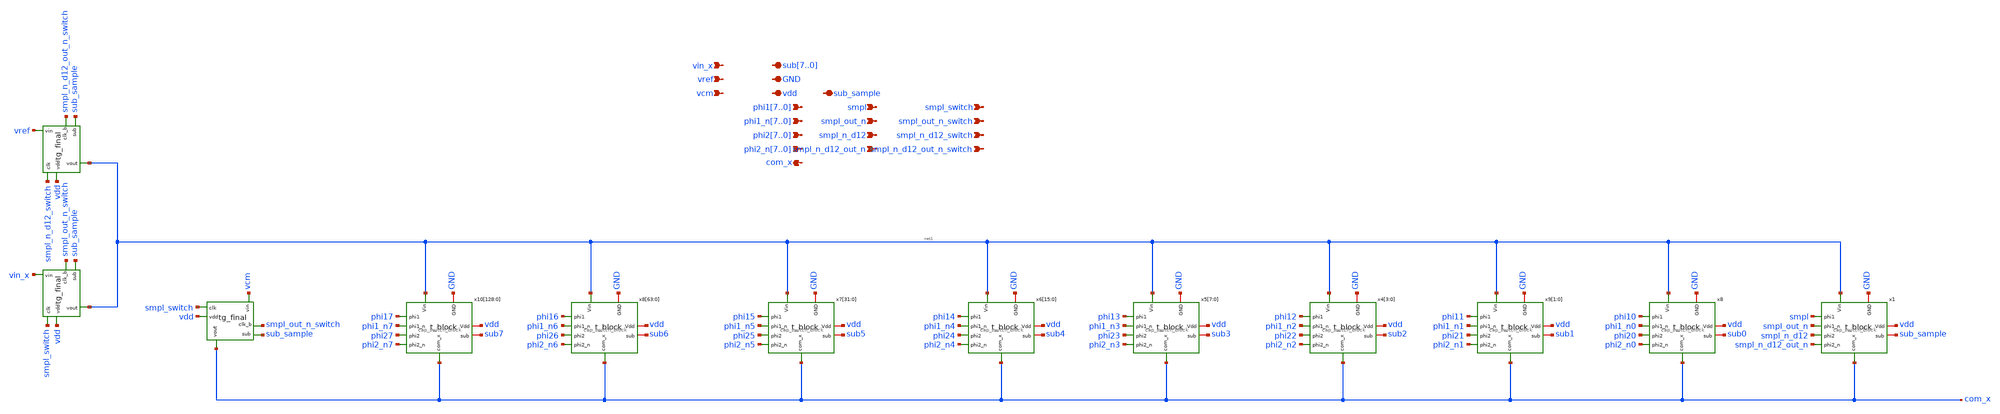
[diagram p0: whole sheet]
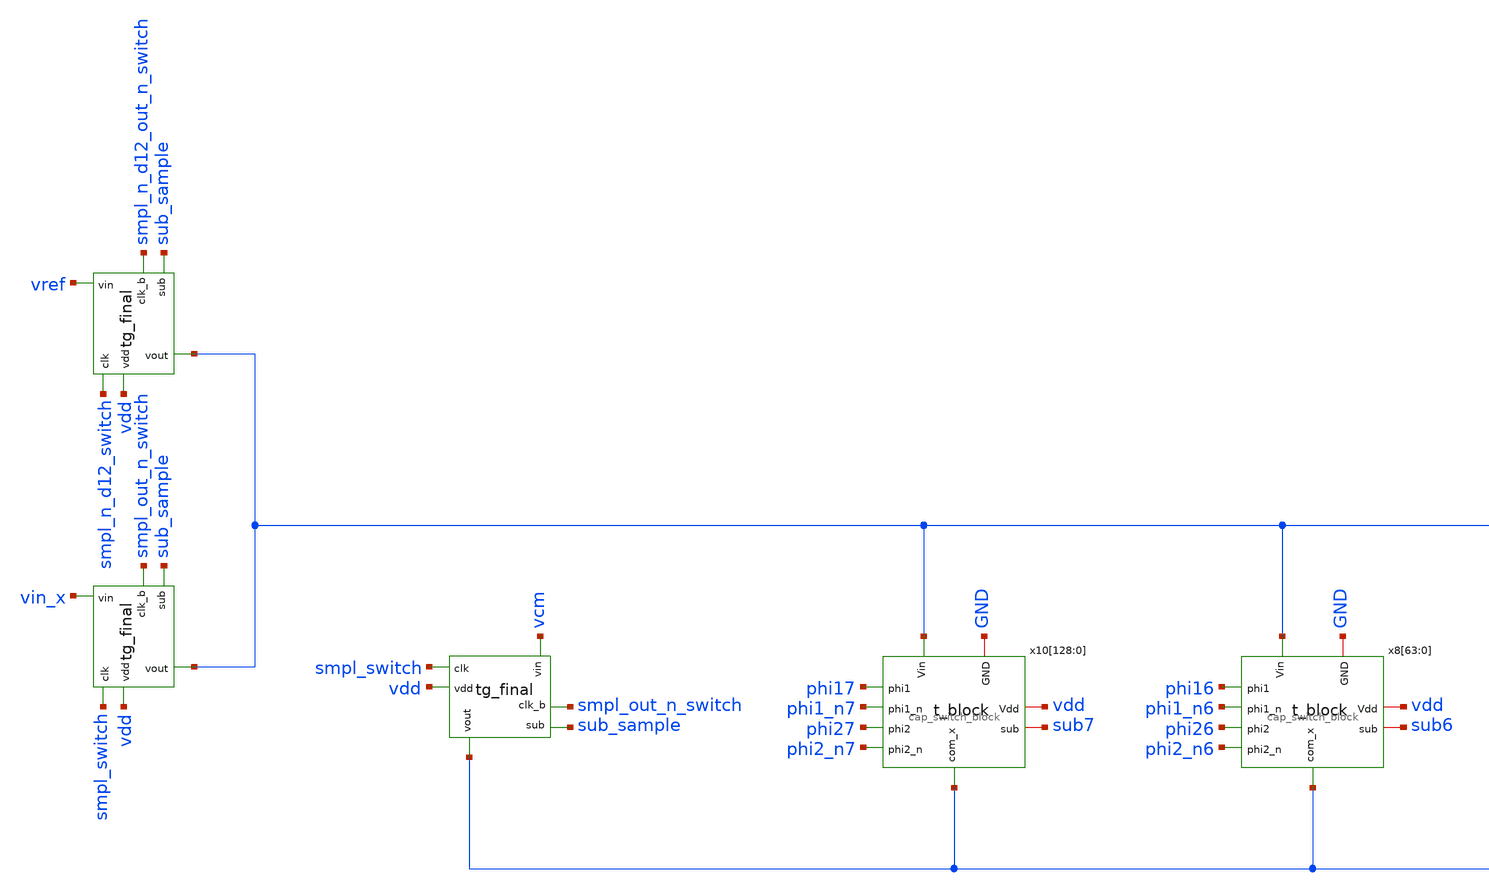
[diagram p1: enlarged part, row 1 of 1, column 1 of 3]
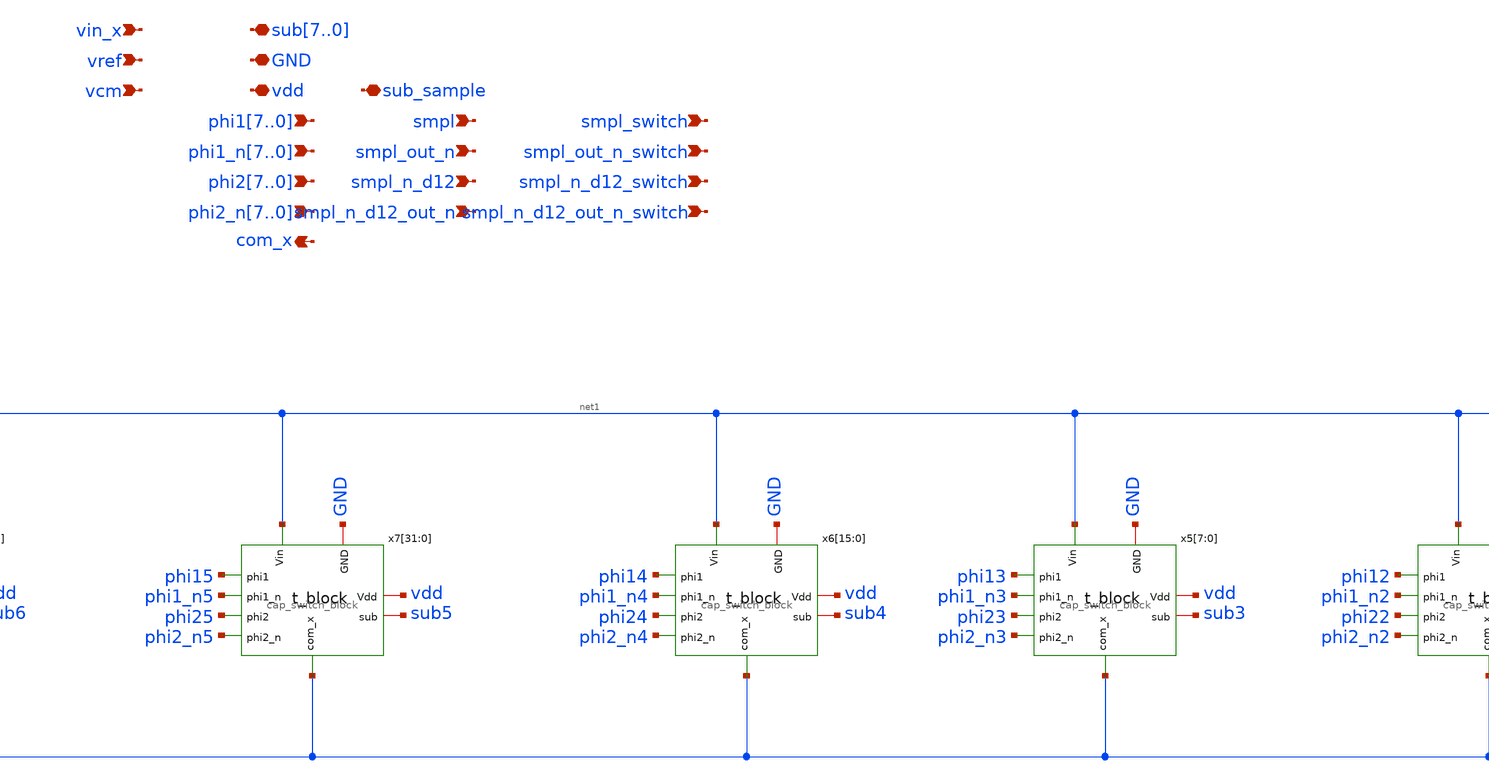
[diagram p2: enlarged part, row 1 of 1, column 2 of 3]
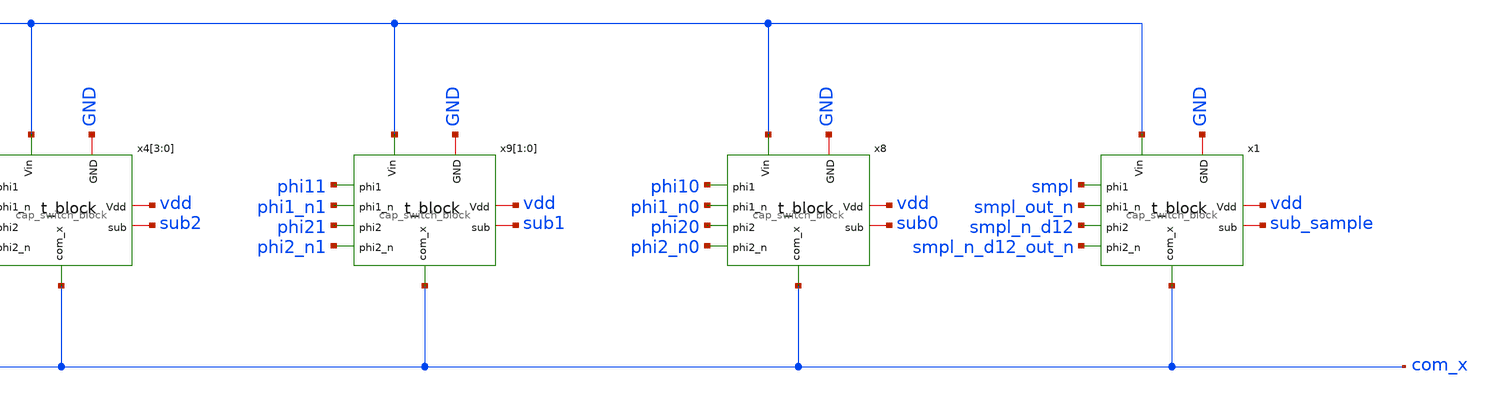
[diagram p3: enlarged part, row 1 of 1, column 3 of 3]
** sch_path: test/design/capdac_switches.sch
**.subckt capdac_switches phi17,phi16,phi15,phi14,phi13,phi12,phi11,phi10
*+ phi1_n7,phi1_n6,phi1_n5,phi1_n4,phi1_n3,phi1_n2,phi1_n1,phi1_n0 vdd GND sub7,sub6,sub5,sub4,sub3,sub2,sub1,sub0 phi27,phi26,phi25,phi24,phi23,phi22,phi21,phi20
*+ phi2_n7,phi2_n6,phi2_n5,phi2_n4,phi2_n3,phi2_n2,phi2_n1,phi2_n0 com_x smpl smpl_out_n smpl_n_d12 smpl_n_d12_out_n sub_sample vcm vref vin_x smpl_switch
*+ smpl_out_n_switch smpl_n_d12_switch smpl_n_d12_out_n_switch
*.ipin phi17,phi16,phi15,phi14,phi13,phi12,phi11,phi10
*.ipin phi1_n7,phi1_n6,phi1_n5,phi1_n4,phi1_n3,phi1_n2,phi1_n1,phi1_n0
*.iopin vdd
*.iopin GND
*.iopin sub7,sub6,sub5,sub4,sub3,sub2,sub1,sub0
*.ipin phi27,phi26,phi25,phi24,phi23,phi22,phi21,phi20
*.ipin phi2_n7,phi2_n6,phi2_n5,phi2_n4,phi2_n3,phi2_n2,phi2_n1,phi2_n0
*.opin com_x
*.ipin smpl
*.ipin smpl_out_n
*.ipin smpl_n_d12
*.ipin smpl_n_d12_out_n
*.iopin sub_sample
*.ipin vcm
*.ipin vref
*.ipin vin_x
*.ipin smpl_switch
*.ipin smpl_out_n_switch
*.ipin smpl_n_d12_switch
*.ipin smpl_n_d12_out_n_switch
x8 net1 sub0 GND vdd phi10 phi20 phi2_n0 phi1_n0 com_x cap_switch_block
x9[1] net1 sub1 GND vdd phi11 phi21 phi2_n1 phi1_n1 com_x cap_switch_block
x9[0] net1 sub1 GND vdd phi11 phi21 phi2_n1 phi1_n1 com_x cap_switch_block
x4[3] net1 sub2 GND vdd phi12 phi22 phi2_n2 phi1_n2 com_x cap_switch_block
x4[2] net1 sub2 GND vdd phi12 phi22 phi2_n2 phi1_n2 com_x cap_switch_block
x4[1] net1 sub2 GND vdd phi12 phi22 phi2_n2 phi1_n2 com_x cap_switch_block
x4[0] net1 sub2 GND vdd phi12 phi22 phi2_n2 phi1_n2 com_x cap_switch_block
x5[7] net1 sub3 GND vdd phi13 phi23 phi2_n3 phi1_n3 com_x cap_switch_block
x5[6] net1 sub3 GND vdd phi13 phi23 phi2_n3 phi1_n3 com_x cap_switch_block
x5[5] net1 sub3 GND vdd phi13 phi23 phi2_n3 phi1_n3 com_x cap_switch_block
x5[4] net1 sub3 GND vdd phi13 phi23 phi2_n3 phi1_n3 com_x cap_switch_block
x5[3] net1 sub3 GND vdd phi13 phi23 phi2_n3 phi1_n3 com_x cap_switch_block
x5[2] net1 sub3 GND vdd phi13 phi23 phi2_n3 phi1_n3 com_x cap_switch_block
x5[1] net1 sub3 GND vdd phi13 phi23 phi2_n3 phi1_n3 com_x cap_switch_block
x5[0] net1 sub3 GND vdd phi13 phi23 phi2_n3 phi1_n3 com_x cap_switch_block
x6[15] net1 sub4 GND vdd phi14 phi24 phi2_n4 phi1_n4 com_x cap_switch_block
x6[14] net1 sub4 GND vdd phi14 phi24 phi2_n4 phi1_n4 com_x cap_switch_block
x6[13] net1 sub4 GND vdd phi14 phi24 phi2_n4 phi1_n4 com_x cap_switch_block
x6[12] net1 sub4 GND vdd phi14 phi24 phi2_n4 phi1_n4 com_x cap_switch_block
x6[11] net1 sub4 GND vdd phi14 phi24 phi2_n4 phi1_n4 com_x cap_switch_block
x6[10] net1 sub4 GND vdd phi14 phi24 phi2_n4 phi1_n4 com_x cap_switch_block
x6[9] net1 sub4 GND vdd phi14 phi24 phi2_n4 phi1_n4 com_x cap_switch_block
x6[8] net1 sub4 GND vdd phi14 phi24 phi2_n4 phi1_n4 com_x cap_switch_block
x6[7] net1 sub4 GND vdd phi14 phi24 phi2_n4 phi1_n4 com_x cap_switch_block
x6[6] net1 sub4 GND vdd phi14 phi24 phi2_n4 phi1_n4 com_x cap_switch_block
x6[5] net1 sub4 GND vdd phi14 phi24 phi2_n4 phi1_n4 com_x cap_switch_block
x6[4] net1 sub4 GND vdd phi14 phi24 phi2_n4 phi1_n4 com_x cap_switch_block
x6[3] net1 sub4 GND vdd phi14 phi24 phi2_n4 phi1_n4 com_x cap_switch_block
x6[2] net1 sub4 GND vdd phi14 phi24 phi2_n4 phi1_n4 com_x cap_switch_block
x6[1] net1 sub4 GND vdd phi14 phi24 phi2_n4 phi1_n4 com_x cap_switch_block
x6[0] net1 sub4 GND vdd phi14 phi24 phi2_n4 phi1_n4 com_x cap_switch_block
x7[31] net1 sub5 GND vdd phi15 phi25 phi2_n5 phi1_n5 com_x cap_switch_block
x7[30] net1 sub5 GND vdd phi15 phi25 phi2_n5 phi1_n5 com_x cap_switch_block
x7[29] net1 sub5 GND vdd phi15 phi25 phi2_n5 phi1_n5 com_x cap_switch_block
x7[28] net1 sub5 GND vdd phi15 phi25 phi2_n5 phi1_n5 com_x cap_switch_block
x7[27] net1 sub5 GND vdd phi15 phi25 phi2_n5 phi1_n5 com_x cap_switch_block
x7[26] net1 sub5 GND vdd phi15 phi25 phi2_n5 phi1_n5 com_x cap_switch_block
x7[25] net1 sub5 GND vdd phi15 phi25 phi2_n5 phi1_n5 com_x cap_switch_block
x7[24] net1 sub5 GND vdd phi15 phi25 phi2_n5 phi1_n5 com_x cap_switch_block
x7[23] net1 sub5 GND vdd phi15 phi25 phi2_n5 phi1_n5 com_x cap_switch_block
x7[22] net1 sub5 GND vdd phi15 phi25 phi2_n5 phi1_n5 com_x cap_switch_block
x7[21] net1 sub5 GND vdd phi15 phi25 phi2_n5 phi1_n5 com_x cap_switch_block
x7[20] net1 sub5 GND vdd phi15 phi25 phi2_n5 phi1_n5 com_x cap_switch_block
x7[19] net1 sub5 GND vdd phi15 phi25 phi2_n5 phi1_n5 com_x cap_switch_block
x7[18] net1 sub5 GND vdd phi15 phi25 phi2_n5 phi1_n5 com_x cap_switch_block
x7[17] net1 sub5 GND vdd phi15 phi25 phi2_n5 phi1_n5 com_x cap_switch_block
x7[16] net1 sub5 GND vdd phi15 phi25 phi2_n5 phi1_n5 com_x cap_switch_block
x7[15] net1 sub5 GND vdd phi15 phi25 phi2_n5 phi1_n5 com_x cap_switch_block
x7[14] net1 sub5 GND vdd phi15 phi25 phi2_n5 phi1_n5 com_x cap_switch_block
x7[13] net1 sub5 GND vdd phi15 phi25 phi2_n5 phi1_n5 com_x cap_switch_block
x7[12] net1 sub5 GND vdd phi15 phi25 phi2_n5 phi1_n5 com_x cap_switch_block
x7[11] net1 sub5 GND vdd phi15 phi25 phi2_n5 phi1_n5 com_x cap_switch_block
x7[10] net1 sub5 GND vdd phi15 phi25 phi2_n5 phi1_n5 com_x cap_switch_block
x7[9] net1 sub5 GND vdd phi15 phi25 phi2_n5 phi1_n5 com_x cap_switch_block
x7[8] net1 sub5 GND vdd phi15 phi25 phi2_n5 phi1_n5 com_x cap_switch_block
x7[7] net1 sub5 GND vdd phi15 phi25 phi2_n5 phi1_n5 com_x cap_switch_block
x7[6] net1 sub5 GND vdd phi15 phi25 phi2_n5 phi1_n5 com_x cap_switch_block
x7[5] net1 sub5 GND vdd phi15 phi25 phi2_n5 phi1_n5 com_x cap_switch_block
x7[4] net1 sub5 GND vdd phi15 phi25 phi2_n5 phi1_n5 com_x cap_switch_block
x7[3] net1 sub5 GND vdd phi15 phi25 phi2_n5 phi1_n5 com_x cap_switch_block
x7[2] net1 sub5 GND vdd phi15 phi25 phi2_n5 phi1_n5 com_x cap_switch_block
x7[1] net1 sub5 GND vdd phi15 phi25 phi2_n5 phi1_n5 com_x cap_switch_block
x7[0] net1 sub5 GND vdd phi15 phi25 phi2_n5 phi1_n5 com_x cap_switch_block
x8[63] net1 sub6 GND vdd phi16 phi26 phi2_n6 phi1_n6 com_x cap_switch_block
x8[62] net1 sub6 GND vdd phi16 phi26 phi2_n6 phi1_n6 com_x cap_switch_block
x8[61] net1 sub6 GND vdd phi16 phi26 phi2_n6 phi1_n6 com_x cap_switch_block
x8[60] net1 sub6 GND vdd phi16 phi26 phi2_n6 phi1_n6 com_x cap_switch_block
x8[59] net1 sub6 GND vdd phi16 phi26 phi2_n6 phi1_n6 com_x cap_switch_block
x8[58] net1 sub6 GND vdd phi16 phi26 phi2_n6 phi1_n6 com_x cap_switch_block
x8[57] net1 sub6 GND vdd phi16 phi26 phi2_n6 phi1_n6 com_x cap_switch_block
x8[56] net1 sub6 GND vdd phi16 phi26 phi2_n6 phi1_n6 com_x cap_switch_block
x8[55] net1 sub6 GND vdd phi16 phi26 phi2_n6 phi1_n6 com_x cap_switch_block
x8[54] net1 sub6 GND vdd phi16 phi26 phi2_n6 phi1_n6 com_x cap_switch_block
x8[53] net1 sub6 GND vdd phi16 phi26 phi2_n6 phi1_n6 com_x cap_switch_block
x8[52] net1 sub6 GND vdd phi16 phi26 phi2_n6 phi1_n6 com_x cap_switch_block
x8[51] net1 sub6 GND vdd phi16 phi26 phi2_n6 phi1_n6 com_x cap_switch_block
x8[50] net1 sub6 GND vdd phi16 phi26 phi2_n6 phi1_n6 com_x cap_switch_block
x8[49] net1 sub6 GND vdd phi16 phi26 phi2_n6 phi1_n6 com_x cap_switch_block
x8[48] net1 sub6 GND vdd phi16 phi26 phi2_n6 phi1_n6 com_x cap_switch_block
x8[47] net1 sub6 GND vdd phi16 phi26 phi2_n6 phi1_n6 com_x cap_switch_block
x8[46] net1 sub6 GND vdd phi16 phi26 phi2_n6 phi1_n6 com_x cap_switch_block
x8[45] net1 sub6 GND vdd phi16 phi26 phi2_n6 phi1_n6 com_x cap_switch_block
x8[44] net1 sub6 GND vdd phi16 phi26 phi2_n6 phi1_n6 com_x cap_switch_block
x8[43] net1 sub6 GND vdd phi16 phi26 phi2_n6 phi1_n6 com_x cap_switch_block
x8[42] net1 sub6 GND vdd phi16 phi26 phi2_n6 phi1_n6 com_x cap_switch_block
x8[41] net1 sub6 GND vdd phi16 phi26 phi2_n6 phi1_n6 com_x cap_switch_block
x8[40] net1 sub6 GND vdd phi16 phi26 phi2_n6 phi1_n6 com_x cap_switch_block
x8[39] net1 sub6 GND vdd phi16 phi26 phi2_n6 phi1_n6 com_x cap_switch_block
x8[38] net1 sub6 GND vdd phi16 phi26 phi2_n6 phi1_n6 com_x cap_switch_block
x8[37] net1 sub6 GND vdd phi16 phi26 phi2_n6 phi1_n6 com_x cap_switch_block
x8[36] net1 sub6 GND vdd phi16 phi26 phi2_n6 phi1_n6 com_x cap_switch_block
x8[35] net1 sub6 GND vdd phi16 phi26 phi2_n6 phi1_n6 com_x cap_switch_block
x8[34] net1 sub6 GND vdd phi16 phi26 phi2_n6 phi1_n6 com_x cap_switch_block
x8[33] net1 sub6 GND vdd phi16 phi26 phi2_n6 phi1_n6 com_x cap_switch_block
x8[32] net1 sub6 GND vdd phi16 phi26 phi2_n6 phi1_n6 com_x cap_switch_block
x8[31] net1 sub6 GND vdd phi16 phi26 phi2_n6 phi1_n6 com_x cap_switch_block
x8[30] net1 sub6 GND vdd phi16 phi26 phi2_n6 phi1_n6 com_x cap_switch_block
x8[29] net1 sub6 GND vdd phi16 phi26 phi2_n6 phi1_n6 com_x cap_switch_block
x8[28] net1 sub6 GND vdd phi16 phi26 phi2_n6 phi1_n6 com_x cap_switch_block
x8[27] net1 sub6 GND vdd phi16 phi26 phi2_n6 phi1_n6 com_x cap_switch_block
x8[26] net1 sub6 GND vdd phi16 phi26 phi2_n6 phi1_n6 com_x cap_switch_block
x8[25] net1 sub6 GND vdd phi16 phi26 phi2_n6 phi1_n6 com_x cap_switch_block
x8[24] net1 sub6 GND vdd phi16 phi26 phi2_n6 phi1_n6 com_x cap_switch_block
x8[23] net1 sub6 GND vdd phi16 phi26 phi2_n6 phi1_n6 com_x cap_switch_block
x8[22] net1 sub6 GND vdd phi16 phi26 phi2_n6 phi1_n6 com_x cap_switch_block
x8[21] net1 sub6 GND vdd phi16 phi26 phi2_n6 phi1_n6 com_x cap_switch_block
x8[20] net1 sub6 GND vdd phi16 phi26 phi2_n6 phi1_n6 com_x cap_switch_block
x8[19] net1 sub6 GND vdd phi16 phi26 phi2_n6 phi1_n6 com_x cap_switch_block
x8[18] net1 sub6 GND vdd phi16 phi26 phi2_n6 phi1_n6 com_x cap_switch_block
x8[17] net1 sub6 GND vdd phi16 phi26 phi2_n6 phi1_n6 com_x cap_switch_block
x8[16] net1 sub6 GND vdd phi16 phi26 phi2_n6 phi1_n6 com_x cap_switch_block
x8[15] net1 sub6 GND vdd phi16 phi26 phi2_n6 phi1_n6 com_x cap_switch_block
x8[14] net1 sub6 GND vdd phi16 phi26 phi2_n6 phi1_n6 com_x cap_switch_block
x8[13] net1 sub6 GND vdd phi16 phi26 phi2_n6 phi1_n6 com_x cap_switch_block
x8[12] net1 sub6 GND vdd phi16 phi26 phi2_n6 phi1_n6 com_x cap_switch_block
x8[11] net1 sub6 GND vdd phi16 phi26 phi2_n6 phi1_n6 com_x cap_switch_block
x8[10] net1 sub6 GND vdd phi16 phi26 phi2_n6 phi1_n6 com_x cap_switch_block
x8[9] net1 sub6 GND vdd phi16 phi26 phi2_n6 phi1_n6 com_x cap_switch_block
x8[8] net1 sub6 GND vdd phi16 phi26 phi2_n6 phi1_n6 com_x cap_switch_block
x8[7] net1 sub6 GND vdd phi16 phi26 phi2_n6 phi1_n6 com_x cap_switch_block
x8[6] net1 sub6 GND vdd phi16 phi26 phi2_n6 phi1_n6 com_x cap_switch_block
x8[5] net1 sub6 GND vdd phi16 phi26 phi2_n6 phi1_n6 com_x cap_switch_block
x8[4] net1 sub6 GND vdd phi16 phi26 phi2_n6 phi1_n6 com_x cap_switch_block
x8[3] net1 sub6 GND vdd phi16 phi26 phi2_n6 phi1_n6 com_x cap_switch_block
x8[2] net1 sub6 GND vdd phi16 phi26 phi2_n6 phi1_n6 com_x cap_switch_block
x8[1] net1 sub6 GND vdd phi16 phi26 phi2_n6 phi1_n6 com_x cap_switch_block
x8[0] net1 sub6 GND vdd phi16 phi26 phi2_n6 phi1_n6 com_x cap_switch_block
x10[128] net1 sub7 GND vdd phi17 phi27 phi2_n7 phi1_n7 com_x cap_switch_block
x10[127] net1 sub7 GND vdd phi17 phi27 phi2_n7 phi1_n7 com_x cap_switch_block
x10[126] net1 sub7 GND vdd phi17 phi27 phi2_n7 phi1_n7 com_x cap_switch_block
x10[125] net1 sub7 GND vdd phi17 phi27 phi2_n7 phi1_n7 com_x cap_switch_block
x10[124] net1 sub7 GND vdd phi17 phi27 phi2_n7 phi1_n7 com_x cap_switch_block
x10[123] net1 sub7 GND vdd phi17 phi27 phi2_n7 phi1_n7 com_x cap_switch_block
x10[122] net1 sub7 GND vdd phi17 phi27 phi2_n7 phi1_n7 com_x cap_switch_block
x10[121] net1 sub7 GND vdd phi17 phi27 phi2_n7 phi1_n7 com_x cap_switch_block
x10[120] net1 sub7 GND vdd phi17 phi27 phi2_n7 phi1_n7 com_x cap_switch_block
x10[119] net1 sub7 GND vdd phi17 phi27 phi2_n7 phi1_n7 com_x cap_switch_block
x10[118] net1 sub7 GND vdd phi17 phi27 phi2_n7 phi1_n7 com_x cap_switch_block
x10[117] net1 sub7 GND vdd phi17 phi27 phi2_n7 phi1_n7 com_x cap_switch_block
x10[116] net1 sub7 GND vdd phi17 phi27 phi2_n7 phi1_n7 com_x cap_switch_block
x10[115] net1 sub7 GND vdd phi17 phi27 phi2_n7 phi1_n7 com_x cap_switch_block
x10[114] net1 sub7 GND vdd phi17 phi27 phi2_n7 phi1_n7 com_x cap_switch_block
x10[113] net1 sub7 GND vdd phi17 phi27 phi2_n7 phi1_n7 com_x cap_switch_block
x10[112] net1 sub7 GND vdd phi17 phi27 phi2_n7 phi1_n7 com_x cap_switch_block
x10[111] net1 sub7 GND vdd phi17 phi27 phi2_n7 phi1_n7 com_x cap_switch_block
x10[110] net1 sub7 GND vdd phi17 phi27 phi2_n7 phi1_n7 com_x cap_switch_block
x10[109] net1 sub7 GND vdd phi17 phi27 phi2_n7 phi1_n7 com_x cap_switch_block
x10[108] net1 sub7 GND vdd phi17 phi27 phi2_n7 phi1_n7 com_x cap_switch_block
x10[107] net1 sub7 GND vdd phi17 phi27 phi2_n7 phi1_n7 com_x cap_switch_block
x10[106] net1 sub7 GND vdd phi17 phi27 phi2_n7 phi1_n7 com_x cap_switch_block
x10[105] net1 sub7 GND vdd phi17 phi27 phi2_n7 phi1_n7 com_x cap_switch_block
x10[104] net1 sub7 GND vdd phi17 phi27 phi2_n7 phi1_n7 com_x cap_switch_block
x10[103] net1 sub7 GND vdd phi17 phi27 phi2_n7 phi1_n7 com_x cap_switch_block
x10[102] net1 sub7 GND vdd phi17 phi27 phi2_n7 phi1_n7 com_x cap_switch_block
x10[101] net1 sub7 GND vdd phi17 phi27 phi2_n7 phi1_n7 com_x cap_switch_block
x10[100] net1 sub7 GND vdd phi17 phi27 phi2_n7 phi1_n7 com_x cap_switch_block
x10[99] net1 sub7 GND vdd phi17 phi27 phi2_n7 phi1_n7 com_x cap_switch_block
x10[98] net1 sub7 GND vdd phi17 phi27 phi2_n7 phi1_n7 com_x cap_switch_block
x10[97] net1 sub7 GND vdd phi17 phi27 phi2_n7 phi1_n7 com_x cap_switch_block
x10[96] net1 sub7 GND vdd phi17 phi27 phi2_n7 phi1_n7 com_x cap_switch_block
x10[95] net1 sub7 GND vdd phi17 phi27 phi2_n7 phi1_n7 com_x cap_switch_block
x10[94] net1 sub7 GND vdd phi17 phi27 phi2_n7 phi1_n7 com_x cap_switch_block
x10[93] net1 sub7 GND vdd phi17 phi27 phi2_n7 phi1_n7 com_x cap_switch_block
x10[92] net1 sub7 GND vdd phi17 phi27 phi2_n7 phi1_n7 com_x cap_switch_block
x10[91] net1 sub7 GND vdd phi17 phi27 phi2_n7 phi1_n7 com_x cap_switch_block
x10[90] net1 sub7 GND vdd phi17 phi27 phi2_n7 phi1_n7 com_x cap_switch_block
x10[89] net1 sub7 GND vdd phi17 phi27 phi2_n7 phi1_n7 com_x cap_switch_block
x10[88] net1 sub7 GND vdd phi17 phi27 phi2_n7 phi1_n7 com_x cap_switch_block
x10[87] net1 sub7 GND vdd phi17 phi27 phi2_n7 phi1_n7 com_x cap_switch_block
x10[86] net1 sub7 GND vdd phi17 phi27 phi2_n7 phi1_n7 com_x cap_switch_block
x10[85] net1 sub7 GND vdd phi17 phi27 phi2_n7 phi1_n7 com_x cap_switch_block
x10[84] net1 sub7 GND vdd phi17 phi27 phi2_n7 phi1_n7 com_x cap_switch_block
x10[83] net1 sub7 GND vdd phi17 phi27 phi2_n7 phi1_n7 com_x cap_switch_block
x10[82] net1 sub7 GND vdd phi17 phi27 phi2_n7 phi1_n7 com_x cap_switch_block
x10[81] net1 sub7 GND vdd phi17 phi27 phi2_n7 phi1_n7 com_x cap_switch_block
x10[80] net1 sub7 GND vdd phi17 phi27 phi2_n7 phi1_n7 com_x cap_switch_block
x10[79] net1 sub7 GND vdd phi17 phi27 phi2_n7 phi1_n7 com_x cap_switch_block
x10[78] net1 sub7 GND vdd phi17 phi27 phi2_n7 phi1_n7 com_x cap_switch_block
x10[77] net1 sub7 GND vdd phi17 phi27 phi2_n7 phi1_n7 com_x cap_switch_block
x10[76] net1 sub7 GND vdd phi17 phi27 phi2_n7 phi1_n7 com_x cap_switch_block
x10[75] net1 sub7 GND vdd phi17 phi27 phi2_n7 phi1_n7 com_x cap_switch_block
x10[74] net1 sub7 GND vdd phi17 phi27 phi2_n7 phi1_n7 com_x cap_switch_block
x10[73] net1 sub7 GND vdd phi17 phi27 phi2_n7 phi1_n7 com_x cap_switch_block
x10[72] net1 sub7 GND vdd phi17 phi27 phi2_n7 phi1_n7 com_x cap_switch_block
x10[71] net1 sub7 GND vdd phi17 phi27 phi2_n7 phi1_n7 com_x cap_switch_block
x10[70] net1 sub7 GND vdd phi17 phi27 phi2_n7 phi1_n7 com_x cap_switch_block
x10[69] net1 sub7 GND vdd phi17 phi27 phi2_n7 phi1_n7 com_x cap_switch_block
x10[68] net1 sub7 GND vdd phi17 phi27 phi2_n7 phi1_n7 com_x cap_switch_block
x10[67] net1 sub7 GND vdd phi17 phi27 phi2_n7 phi1_n7 com_x cap_switch_block
x10[66] net1 sub7 GND vdd phi17 phi27 phi2_n7 phi1_n7 com_x cap_switch_block
x10[65] net1 sub7 GND vdd phi17 phi27 phi2_n7 phi1_n7 com_x cap_switch_block
x10[64] net1 sub7 GND vdd phi17 phi27 phi2_n7 phi1_n7 com_x cap_switch_block
x10[63] net1 sub7 GND vdd phi17 phi27 phi2_n7 phi1_n7 com_x cap_switch_block
x10[62] net1 sub7 GND vdd phi17 phi27 phi2_n7 phi1_n7 com_x cap_switch_block
x10[61] net1 sub7 GND vdd phi17 phi27 phi2_n7 phi1_n7 com_x cap_switch_block
x10[60] net1 sub7 GND vdd phi17 phi27 phi2_n7 phi1_n7 com_x cap_switch_block
x10[59] net1 sub7 GND vdd phi17 phi27 phi2_n7 phi1_n7 com_x cap_switch_block
x10[58] net1 sub7 GND vdd phi17 phi27 phi2_n7 phi1_n7 com_x cap_switch_block
x10[57] net1 sub7 GND vdd phi17 phi27 phi2_n7 phi1_n7 com_x cap_switch_block
x10[56] net1 sub7 GND vdd phi17 phi27 phi2_n7 phi1_n7 com_x cap_switch_block
x10[55] net1 sub7 GND vdd phi17 phi27 phi2_n7 phi1_n7 com_x cap_switch_block
x10[54] net1 sub7 GND vdd phi17 phi27 phi2_n7 phi1_n7 com_x cap_switch_block
x10[53] net1 sub7 GND vdd phi17 phi27 phi2_n7 phi1_n7 com_x cap_switch_block
x10[52] net1 sub7 GND vdd phi17 phi27 phi2_n7 phi1_n7 com_x cap_switch_block
x10[51] net1 sub7 GND vdd phi17 phi27 phi2_n7 phi1_n7 com_x cap_switch_block
x10[50] net1 sub7 GND vdd phi17 phi27 phi2_n7 phi1_n7 com_x cap_switch_block
x10[49] net1 sub7 GND vdd phi17 phi27 phi2_n7 phi1_n7 com_x cap_switch_block
x10[48] net1 sub7 GND vdd phi17 phi27 phi2_n7 phi1_n7 com_x cap_switch_block
x10[47] net1 sub7 GND vdd phi17 phi27 phi2_n7 phi1_n7 com_x cap_switch_block
x10[46] net1 sub7 GND vdd phi17 phi27 phi2_n7 phi1_n7 com_x cap_switch_block
x10[45] net1 sub7 GND vdd phi17 phi27 phi2_n7 phi1_n7 com_x cap_switch_block
x10[44] net1 sub7 GND vdd phi17 phi27 phi2_n7 phi1_n7 com_x cap_switch_block
x10[43] net1 sub7 GND vdd phi17 phi27 phi2_n7 phi1_n7 com_x cap_switch_block
x10[42] net1 sub7 GND vdd phi17 phi27 phi2_n7 phi1_n7 com_x cap_switch_block
x10[41] net1 sub7 GND vdd phi17 phi27 phi2_n7 phi1_n7 com_x cap_switch_block
x10[40] net1 sub7 GND vdd phi17 phi27 phi2_n7 phi1_n7 com_x cap_switch_block
x10[39] net1 sub7 GND vdd phi17 phi27 phi2_n7 phi1_n7 com_x cap_switch_block
x10[38] net1 sub7 GND vdd phi17 phi27 phi2_n7 phi1_n7 com_x cap_switch_block
x10[37] net1 sub7 GND vdd phi17 phi27 phi2_n7 phi1_n7 com_x cap_switch_block
x10[36] net1 sub7 GND vdd phi17 phi27 phi2_n7 phi1_n7 com_x cap_switch_block
x10[35] net1 sub7 GND vdd phi17 phi27 phi2_n7 phi1_n7 com_x cap_switch_block
x10[34] net1 sub7 GND vdd phi17 phi27 phi2_n7 phi1_n7 com_x cap_switch_block
x10[33] net1 sub7 GND vdd phi17 phi27 phi2_n7 phi1_n7 com_x cap_switch_block
x10[32] net1 sub7 GND vdd phi17 phi27 phi2_n7 phi1_n7 com_x cap_switch_block
x10[31] net1 sub7 GND vdd phi17 phi27 phi2_n7 phi1_n7 com_x cap_switch_block
x10[30] net1 sub7 GND vdd phi17 phi27 phi2_n7 phi1_n7 com_x cap_switch_block
x10[29] net1 sub7 GND vdd phi17 phi27 phi2_n7 phi1_n7 com_x cap_switch_block
x10[28] net1 sub7 GND vdd phi17 phi27 phi2_n7 phi1_n7 com_x cap_switch_block
x10[27] net1 sub7 GND vdd phi17 phi27 phi2_n7 phi1_n7 com_x cap_switch_block
x10[26] net1 sub7 GND vdd phi17 phi27 phi2_n7 phi1_n7 com_x cap_switch_block
x10[25] net1 sub7 GND vdd phi17 phi27 phi2_n7 phi1_n7 com_x cap_switch_block
x10[24] net1 sub7 GND vdd phi17 phi27 phi2_n7 phi1_n7 com_x cap_switch_block
x10[23] net1 sub7 GND vdd phi17 phi27 phi2_n7 phi1_n7 com_x cap_switch_block
x10[22] net1 sub7 GND vdd phi17 phi27 phi2_n7 phi1_n7 com_x cap_switch_block
x10[21] net1 sub7 GND vdd phi17 phi27 phi2_n7 phi1_n7 com_x cap_switch_block
x10[20] net1 sub7 GND vdd phi17 phi27 phi2_n7 phi1_n7 com_x cap_switch_block
x10[19] net1 sub7 GND vdd phi17 phi27 phi2_n7 phi1_n7 com_x cap_switch_block
x10[18] net1 sub7 GND vdd phi17 phi27 phi2_n7 phi1_n7 com_x cap_switch_block
x10[17] net1 sub7 GND vdd phi17 phi27 phi2_n7 phi1_n7 com_x cap_switch_block
x10[16] net1 sub7 GND vdd phi17 phi27 phi2_n7 phi1_n7 com_x cap_switch_block
x10[15] net1 sub7 GND vdd phi17 phi27 phi2_n7 phi1_n7 com_x cap_switch_block
x10[14] net1 sub7 GND vdd phi17 phi27 phi2_n7 phi1_n7 com_x cap_switch_block
x10[13] net1 sub7 GND vdd phi17 phi27 phi2_n7 phi1_n7 com_x cap_switch_block
x10[12] net1 sub7 GND vdd phi17 phi27 phi2_n7 phi1_n7 com_x cap_switch_block
x10[11] net1 sub7 GND vdd phi17 phi27 phi2_n7 phi1_n7 com_x cap_switch_block
x10[10] net1 sub7 GND vdd phi17 phi27 phi2_n7 phi1_n7 com_x cap_switch_block
x10[9] net1 sub7 GND vdd phi17 phi27 phi2_n7 phi1_n7 com_x cap_switch_block
x10[8] net1 sub7 GND vdd phi17 phi27 phi2_n7 phi1_n7 com_x cap_switch_block
x10[7] net1 sub7 GND vdd phi17 phi27 phi2_n7 phi1_n7 com_x cap_switch_block
x10[6] net1 sub7 GND vdd phi17 phi27 phi2_n7 phi1_n7 com_x cap_switch_block
x10[5] net1 sub7 GND vdd phi17 phi27 phi2_n7 phi1_n7 com_x cap_switch_block
x10[4] net1 sub7 GND vdd phi17 phi27 phi2_n7 phi1_n7 com_x cap_switch_block
x10[3] net1 sub7 GND vdd phi17 phi27 phi2_n7 phi1_n7 com_x cap_switch_block
x10[2] net1 sub7 GND vdd phi17 phi27 phi2_n7 phi1_n7 com_x cap_switch_block
x10[1] net1 sub7 GND vdd phi17 phi27 phi2_n7 phi1_n7 com_x cap_switch_block
x10[0] net1 sub7 GND vdd phi17 phi27 phi2_n7 phi1_n7 com_x cap_switch_block
x1 net1 sub_sample GND vdd smpl smpl_n_d12 smpl_n_d12_out_n smpl_out_n com_x cap_switch_block
x210 smpl_switch sub_sample com_x vcm vdd smpl_out_n_switch tg_final
x29 smpl_switch sub_sample com_x vcm vdd smpl_out_n_switch tg_final
x28 smpl_switch sub_sample com_x vcm vdd smpl_out_n_switch tg_final
x27 smpl_switch sub_sample com_x vcm vdd smpl_out_n_switch tg_final
x26 smpl_switch sub_sample com_x vcm vdd smpl_out_n_switch tg_final
x25 smpl_switch sub_sample com_x vcm vdd smpl_out_n_switch tg_final
x24 smpl_switch sub_sample com_x vcm vdd smpl_out_n_switch tg_final
x23 smpl_switch sub_sample com_x vcm vdd smpl_out_n_switch tg_final
x22 smpl_switch sub_sample com_x vcm vdd smpl_out_n_switch tg_final
x21 smpl_switch sub_sample com_x vcm vdd smpl_out_n_switch tg_final
x20 smpl_switch sub_sample com_x vcm vdd smpl_out_n_switch tg_final
x310 smpl_switch sub_sample net1 vin_x vdd smpl_out_n_switch tg_final
x39 smpl_switch sub_sample net1 vin_x vdd smpl_out_n_switch tg_final
x38 smpl_switch sub_sample net1 vin_x vdd smpl_out_n_switch tg_final
x37 smpl_switch sub_sample net1 vin_x vdd smpl_out_n_switch tg_final
x36 smpl_switch sub_sample net1 vin_x vdd smpl_out_n_switch tg_final
x35 smpl_switch sub_sample net1 vin_x vdd smpl_out_n_switch tg_final
x34 smpl_switch sub_sample net1 vin_x vdd smpl_out_n_switch tg_final
x33 smpl_switch sub_sample net1 vin_x vdd smpl_out_n_switch tg_final
x32 smpl_switch sub_sample net1 vin_x vdd smpl_out_n_switch tg_final
x31 smpl_switch sub_sample net1 vin_x vdd smpl_out_n_switch tg_final
x30 smpl_switch sub_sample net1 vin_x vdd smpl_out_n_switch tg_final
x410 smpl_n_d12_switch sub_sample net1 vref vdd smpl_n_d12_out_n_switch tg_final
x49 smpl_n_d12_switch sub_sample net1 vref vdd smpl_n_d12_out_n_switch tg_final
x48 smpl_n_d12_switch sub_sample net1 vref vdd smpl_n_d12_out_n_switch tg_final
x47 smpl_n_d12_switch sub_sample net1 vref vdd smpl_n_d12_out_n_switch tg_final
x46 smpl_n_d12_switch sub_sample net1 vref vdd smpl_n_d12_out_n_switch tg_final
x45 smpl_n_d12_switch sub_sample net1 vref vdd smpl_n_d12_out_n_switch tg_final
x44 smpl_n_d12_switch sub_sample net1 vref vdd smpl_n_d12_out_n_switch tg_final
x43 smpl_n_d12_switch sub_sample net1 vref vdd smpl_n_d12_out_n_switch tg_final
x42 smpl_n_d12_switch sub_sample net1 vref vdd smpl_n_d12_out_n_switch tg_final
x41 smpl_n_d12_switch sub_sample net1 vref vdd smpl_n_d12_out_n_switch tg_final
x40 smpl_n_d12_switch sub_sample net1 vref vdd smpl_n_d12_out_n_switch tg_final
**.ends

* expanding   symbol:  cap_switch_block.sym # of pins=9
** sym_path: test/design/cap_switch_block.sym
** sch_path: test/design/cap_switch_block.sch
.subckt cap_switch_block Vin sub GND Vdd phi1 phi2 phi2_n phi1_n com_x
*.ipin Vin
*.opin com_x
*.ipin phi1
*.ipin phi1_n
*.iopin Vdd
*.iopin GND
*.iopin sub
*.ipin phi2
*.ipin phi2_n
XC9 com_x net1 sky130_fd_pr__cap_mim_m3_1 W=7 L=7 MF=1 m=1
x4 phi1 sub net1 Vin Vdd phi1_n tg_final
x1 phi2 sub net1 GND Vdd phi2_n tg_final
.ends


* expanding   symbol:  final/tg_final.sym # of pins=6
** sym_path: top/test/design/tg_final.sym
** sch_path: top/test/design/tg_final.sch
.subckt tg_final clk sub vout vin vdd clk_b
*.ipin clk
*.ipin vin
*.opin vout
*.ipin vdd
*.ipin sub
*.ipin clk_b
XM2 vout clk vin sub sky130_fd_pr__nfet_01v8 L=0.15 W=1 nf=1 ad='int((nf+1)/2) * W/nf * 0.29' as='int((nf+2)/2) * W/nf * 0.29'
+ pd='2*int((nf+1)/2) * (W/nf + 0.29)' ps='2*int((nf+2)/2) * (W/nf + 0.29)' nrd='0.29 / W' nrs='0.29 / W'
+ sa=0 sb=0 sd=0 mult=1 m=1
XM1 vout clk_b vin vdd sky130_fd_pr__pfet_01v8 L=0.15 W=1 nf=1 ad='int((nf+1)/2) * W/nf * 0.29' as='int((nf+2)/2) * W/nf * 0.29'
+ pd='2*int((nf+1)/2) * (W/nf + 0.29)' ps='2*int((nf+2)/2) * (W/nf + 0.29)' nrd='0.29 / W' nrs='0.29 / W'
+ sa=0 sb=0 sd=0 mult=1 m=1
.ends

.end
